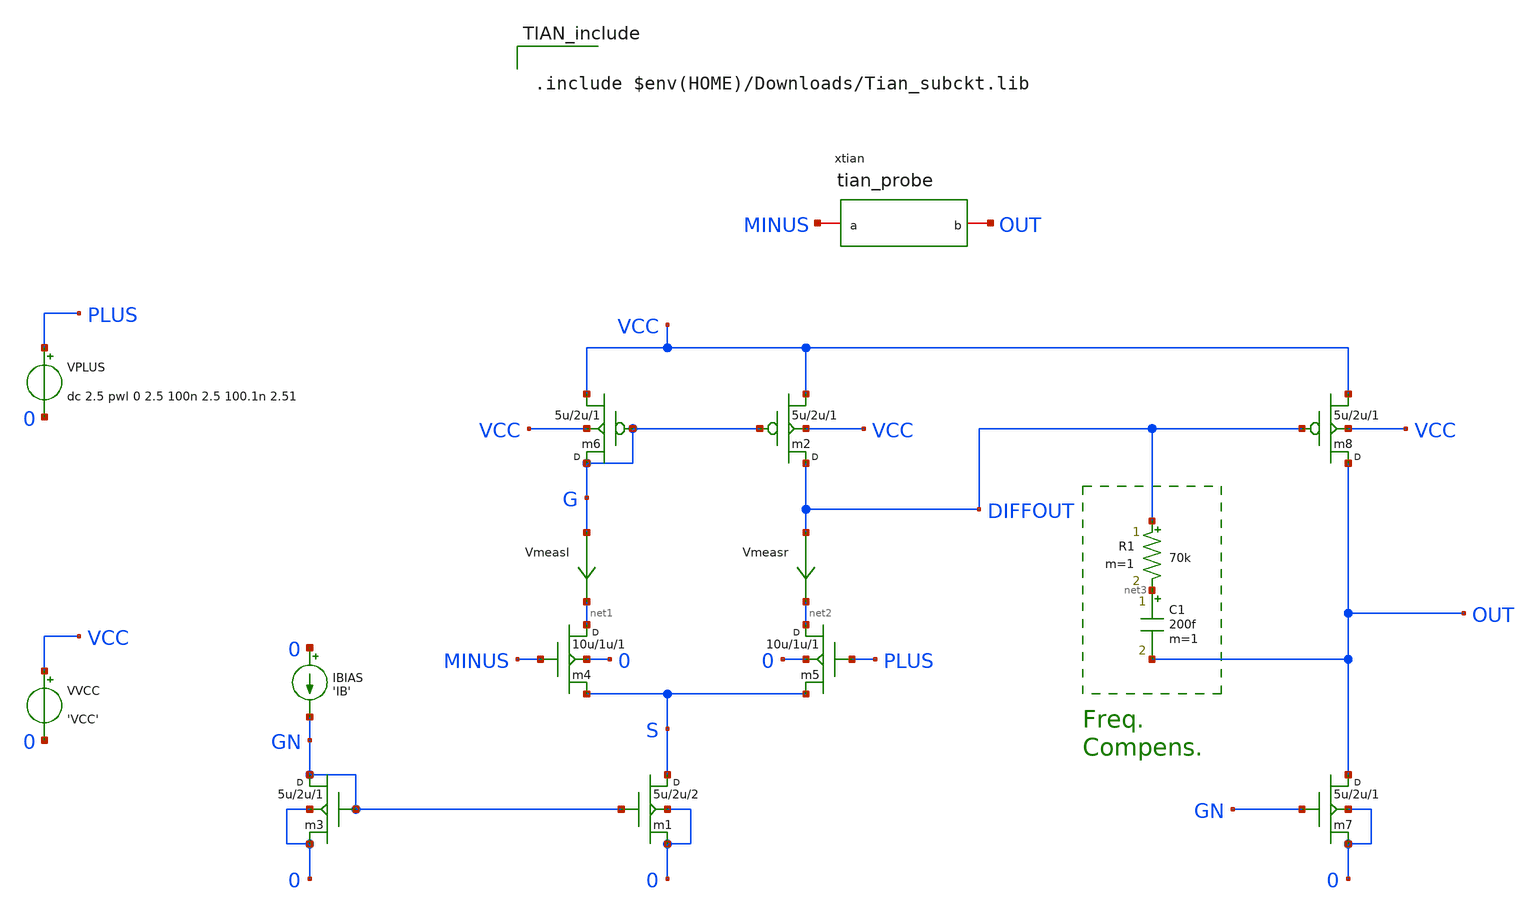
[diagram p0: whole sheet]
** sch_path: schema/tian_probe/test_tian.sch
* Copyright (C) 1998-2024 Stefan Frederik Schippers
* This program is free software; you can redistribute it and/or modify
* it under the terms of the GNU General Public License as published by
* the Free Software Foundation; either version 2 of the License, or
* (at your option) any later version.
* This program is distributed in the hope that it will be useful,
* but WITHOUT ANY WARRANTY; without even the implied warranty of
* MERCHANTABILITY or FITNESS FOR A PARTICULAR PURPOSE.  See the
* GNU General Public License for more details.
* You should have received a copy of the GNU General Public License
* along with this program; if not, write to the Free Software
**.subckt test_tian
m1 S GN 0 0 cmosn w=5u l=2u m=2
m2 DIFFOUT G VCC VCC cmosp w=5u l=2u m=1
VVCC VCC 0 'VCC'
m3 GN GN 0 0 cmosn w=5u l=2u m=1
IBIAS 0 GN 'IB'
m4 net1 MINUS S 0 cmosn w=10u l=1u m=1
m5 net2 PLUS S 0 cmosn w=10u l=1u m=1
m6 G G VCC VCC cmosp w=5u l=2u m=1
VPLUS PLUS 0 dc 2.5 pwl 0 2.5 100n 2.5 100.1n 2.51
Vmeasr DIFFOUT net2 0
.save i(vmeasr)
Vmeasl G net1 0
.save i(vmeasl)
m7 OUT GN 0 0 cmosn w=5u l=2u m=1
m8 OUT DIFFOUT VCC VCC cmosp w=5u l=2u m=1
R1 DIFFOUT net3 70k m=1
C1 net3 OUT 200f m=1
xtian OUT MINUS tian_probe
**** begin user architecture code


.temp 30
.param IB=2u GMIN=1e-16
.param VCC = 5
.option savecurrents
.control
   set filetype=ascii
   save all
   op
   remzerovec
   write test_tian.raw
   set appendwrite

   * First AC Tian set
   ac dec 10 0.1 100MEG

   * Second AC Tian set
   alter I.xtian.Ii acmag=1
   alter V.xtian.Vi acmag=0
   ac dec 10 0.1 100MEG

   *Function from Tian.lib
   let tian_signal = tian_loop()
   let dbsignal =  db(tian_signal)
   let tphase = 180*cph(tian_signal)/pi

   *GBWP
   meas ac zerogainfreq WHEN dbsignal=0
   *PM
   meas ac phaseatzerogain FIND tphase AT=zerogainfreq

   write test_tian.raw dbsignal tphase zerogainfreq phaseatzerogain

   plot dbsignal
   plot tphase

   *quit 0
.endc





.include $env(HOME)/Downloads/Tian_subckt.lib


**** end user architecture code
**.ends

* expanding   symbol:  /home/alberto/Downloads/tian_probe.sym # of pins=2
** sym_path: schema/tian_probe/tian_probe.sym
** sch_path: schema/tian_probe/tian_probe.sch
.subckt tian_probe b a
*.iopin a
*.iopin b
Vi x a 0 AC 1
Ii 0 x 0 AC 0
Vnodebuffer b x 0
.ends

**** begin user architecture code

*p-ch model
.MODEL CMOSP PMOS ( LEVEL   = 49             acm     = 3 VERSION = 3.1            TNOM    = 27
+             TOX     = 7.7E-9 XJ      = 1E-7           NCH     = 8.52E16        VTH0    = -0.6897992 K1      =
+ 0.4134289      K2      = -5.342989E-3   K3      = 24.8361788 K3B     = -1.4390847     W0      = 2.467689E-6
+    NLX     = 3.096223E-7 DVT0W   = 0              DVT1W   = 0              DVT2W   = 0 DVT0    = 1.3209807
+      DVT1    = 0.4695965      DVT2    = -8.790762E-4 U0      = 150.6275733    UA      = 2.016943E-10   UB
+      = 1.714919E-18 UC      = -1.36948E-11   VSAT    = 9.559222E4     A0      = 0.9871247 AGS     =
+ 0.3541967      B0      = 3.188091E-6    B1      = 5E-6 KETA    = -0.0169877     A1      = 0              A2
+      = 1 RDSW    = 2.443009E3     PRWG    = 0.0260616      PRWB    = 0.141561 WR      = 1
+              WINT    = 5.038936E-8    LINT    = 1.650588E-9 XL      = -2E-8          XW      = 0              DWG
+     = -1.535456E-8 DWB     = 1.256904E-8    VOFF    = -0.15          NFACTOR = 1.5460516 CIT     = 0
+              CDSC    = 1.413317E-4    CDSCD   = 0 CDSCB   = 0              ETA0    = 0.3751392      ETAB    =
+ 2.343374E-3 DSUB    = 0.8877574      PCLM    = 5.8638076      PDIBLC1 = 1.05224E-3 PDIBLC2 = 3.481753E-5
+    PDIBLCB = 2.37525E-3     DROUT   = 0.0277454 PSCBE1  = 3.013379E10    PSCBE2  = 3.608179E-8    PVAG    =
+ 3.9564294 DELTA   = 0.01           MOBMOD  = 1              PRT     = 0 UTE     = -1.5           KT1     =
+ -0.11          KT1L    = 0 KT2     = 0.022          UA1     = 4.31E-9        UB1     = -7.61E-18 UC1
+     = -5.6E-11       AT      = 3.3E4          WL      = 0 WLN     = 1              WW      = -5.22182E-16
+   WWN     = 1.125 WWL     = 0              LL      = 0              LLN     = 1 LW      = 0
+              LWN     = 1              LWL     = 0 CAPMOD  = 2              XPART   = 0.4            CGDO    =
+ 2.307E-10 CGSO    = 2.307E-10      CGBO    = 0              CJ      = 1.397645E-3 PB      = 0.99           MJ
+      = 0.5574537      CJSW    = 3.665392E-10 PBSW    = 0.99           MJSW    = 0.3399328      PVTH0   =
+ 0.0114364 PRDSW   = 52.7951169     PK2     = 9.714153E-4    WKETA   = 0.0109418 LKETA   = 7.702974E-3     )


*n-ch model
.MODEL CMOSN NMOS ( LEVEL   = 49             acm     = 3 VERSION = 3.1            TNOM    = 27
+             TOX     = 7.7E-9 XJ      = 1E-7           NCH     = 2.3579E17      VTH0    = 0.5048265 K1      =
+ 0.5542796      K2      = 0.0155863      K3      = 2.3475646 K3B     = -3.3142916     W0      = 4.145888E-5
+    NLX     = 1.430868E-7 DVT0W   = 0              DVT1W   = 0              DVT2W   = 0 DVT0    =
+ -0.0150839     DVT1    = 1.51022E-3     DVT2    = 0.170688 U0      = 415.8570638    UA      = 5.057324E-11
+   UB      = 1.496793E-18 UC      = 2.986268E-11   VSAT    = 1.237033E5     A0      = 0.9098788 AGS     =
+ 0.2120181      B0      = 1.683612E-6    B1      = 5E-6 KETA    = -4.011887E-4   A1      = 0              A2
+      = 1 RDSW    = 1.156967E3     PRWG    = -8.468558E-3   PRWB    = -7.678669E-3 WR      = 1
+              WINT    = 5.621821E-8    LINT    = 1.606205E-8 XL      = -2E-8          XW      = 0              DWG
+     = -6.450939E-9 DWB     = 6.530228E-9    VOFF    = -0.1259348     NFACTOR = 0.3344887 CIT     = 0
+              CDSC    = 1.527511E-3    CDSCD   = 0 CDSCB   = 0              ETA0    = 1.21138E-3     ETAB    =
+ -1.520242E-4 DSUB    = 0.1259886      PCLM    = 0.8254768      PDIBLC1 = 0.4211084 PDIBLC2 = 6.081164E-3
+    PDIBLCB = -5.865856E-6   DROUT   = 0.7022263 PSCBE1  = 7.238634E9     PSCBE2  = 5E-10          PVAG    =
+ 0.6261655 DELTA   = 0.01           MOBMOD  = 1              PRT     = 0 UTE     = -1.5           KT1     =
+ -0.11          KT1L    = 0 KT2     = 0.022          UA1     = 4.31E-9        UB1     = -7.61E-18 UC1
+     = -5.6E-11       AT      = 3.3E4          WL      = 0 WLN     = 1              WW      = -1.22182E-15
+   WWN     = 1.137 WWL     = 0              LL      = 0              LLN     = 1 LW      = 0
+              LWN     = 1              LWL     = 0 CAPMOD  = 2              XPART   = 0.4            CGDO    =
+ 1.96E-10 CGSO    = 1.96E-10       CGBO    = 0              CJ      = 8.829973E-4 PB      = 0.7946332      MJ
+      = 0.3539285      CJSW    = 2.992362E-10 PBSW    = 0.9890846      MJSW    = 0.1871372      PVTH0   =
+ -0.0148617 PRDSW   = -114.7860236   PK2     = -5.151187E-3   WKETA   = 5.687313E-3 LKETA   = -0.018518       )

**** end user architecture code
.end
